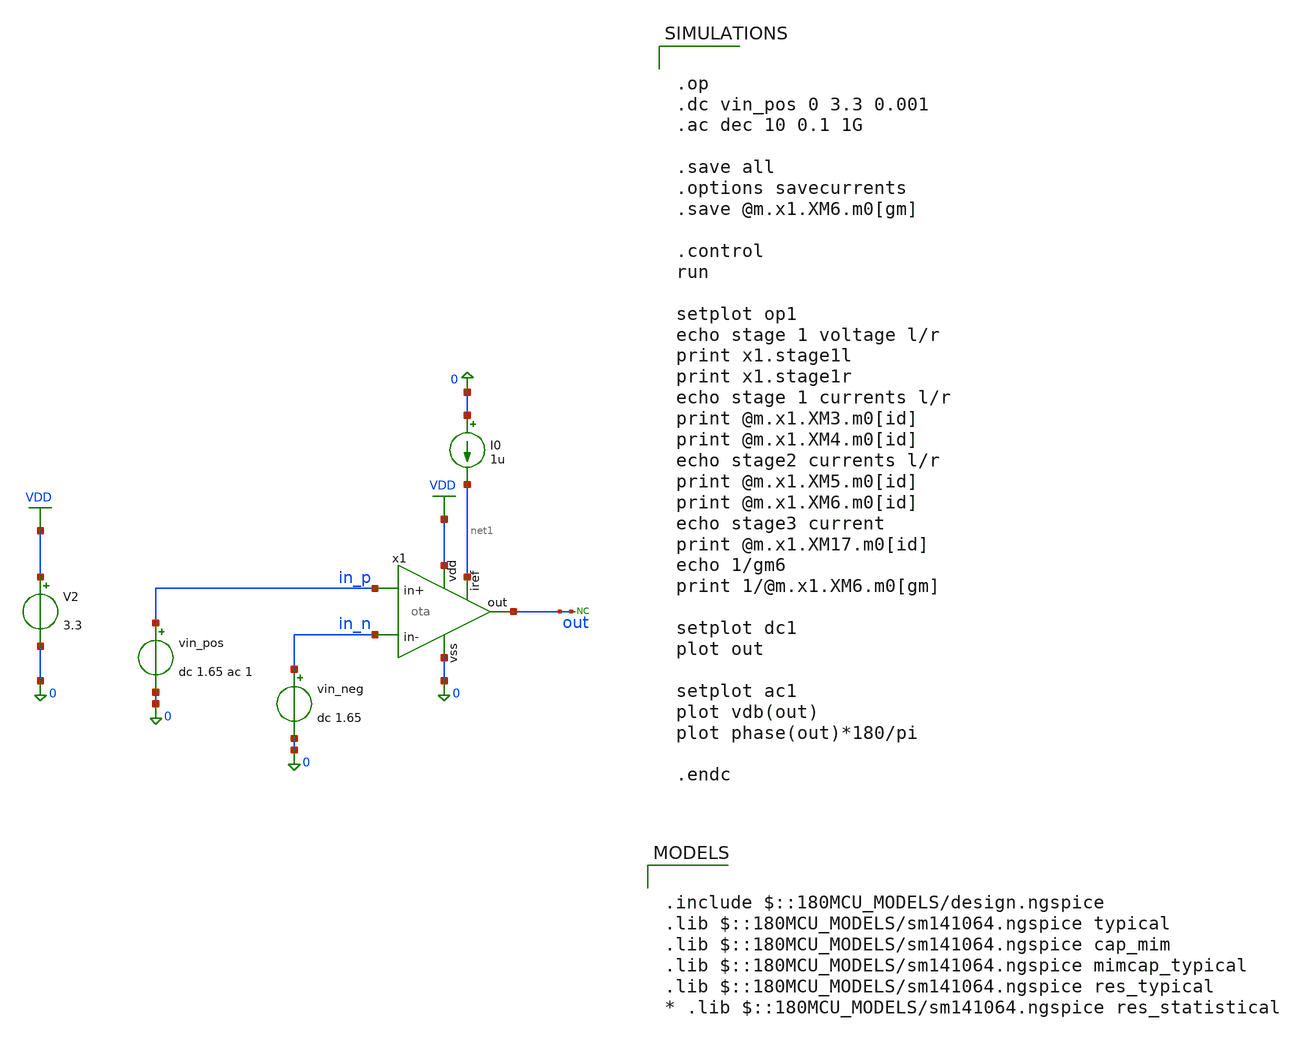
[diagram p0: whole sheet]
** sch_path: General/ADC/OTA/ota_tb.sch
**.subckt ota_tb
vin_pos in_p 0 dc 1.65 ac 1
V2 VDD 0 3.3
.save i(v2)
* noconn out
vin_neg in_n 0 dc 1.65
I0 0 net1 1u
x1 out in_n in_p VDD 0 net1 ota
**** begin user architecture code

.include $::180MCU_MODELS/design.ngspice
.lib $::180MCU_MODELS/sm141064.ngspice typical
.lib $::180MCU_MODELS/sm141064.ngspice cap_mim
.lib $::180MCU_MODELS/sm141064.ngspice mimcap_typical
.lib $::180MCU_MODELS/sm141064.ngspice res_typical
* .lib $::180MCU_MODELS/sm141064.ngspice res_statistical



.op
.dc vin_pos 0 3.3 0.001
.ac dec 10 0.1 1G

.save all
.options savecurrents
.save @m.x1.XM6.m0[gm]

.control
run

setplot op1
echo stage 1 voltage l/r
print x1.stage1l
print x1.stage1r
echo stage 1 currents l/r
print @m.x1.XM3.m0[id]
print @m.x1.XM4.m0[id]
echo stage2 currents l/r
print @m.x1.XM5.m0[id]
print @m.x1.XM6.m0[id]
echo stage3 current
print @m.x1.XM17.m0[id]
echo 1/gm6
print 1/@m.x1.XM6.m0[gm]

setplot dc1
plot out

setplot ac1
plot vdb(out)
plot phase(out)*180/pi

.endc


**** end user architecture code
**.ends
.GLOBAL VDD
.end
